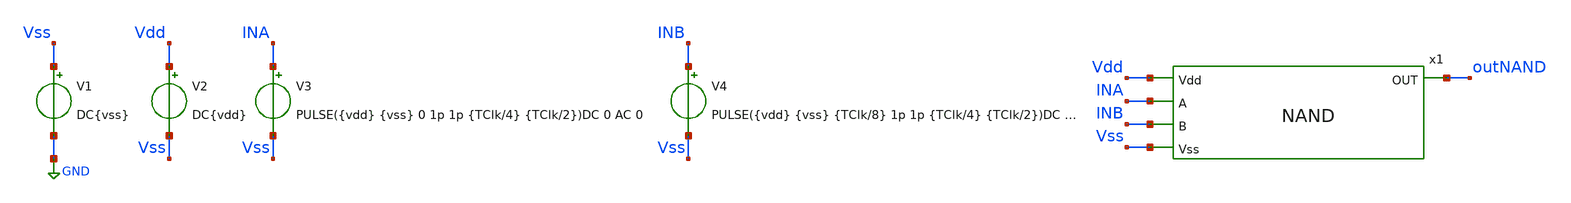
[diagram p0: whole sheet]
** sch_path: icdesign/sch/NAND/tb_NAND.sch
**.subckt tb_NAND
V1 Vss GND DC{vss}
V2 Vdd Vss DC{vdd}
V3 INA Vss PULSE({vdd} {vss} 0 1p 1p {TClk/4} {TClk/2})DC 0 AC 0
V4 INB Vss PULSE({vdd} {vss} {TClk/8} 1p 1p {TClk/4} {TClk/2})DC 0 AC 0
x1 Vdd INA INB outNAND Vss NAND
**** begin user architecture code





* Circuit Parameters
.param vdd  = 1.8
.param vss  = 0.0
.param Tclk = 10n
.options TEMP = 65.0


* Include Models
.lib ~/skywater/skywater-pdk/libraries/sky130_fd_pr_ngspice/latest/models/corners/sky130.lib TT


* OP Parameters & Singals to save
.save all


*Simulations
.control
  tran 0.01u 100n
  setplot tran1
  plot v(INA)v(INB)+2 v(outNAND)+4
.endc
.end


**** end user architecture code
**.ends

* expanding   symbol:  NAND/NAND.sym # of pins=5
** sym_path: icdesign/sch/NAND/NAND.sym
** sch_path: icdesign/sch/NAND/NAND.sch
.subckt NAND Vdd A B OUT Vss
*.ipin A
*.ipin B
*.ipin Vdd
*.ipin Vss
*.opin OUT
XM1 net1 B Vss Vss sky130_fd_pr__nfet_01v8 L=0.15 W=0.75 nf=1 ad='int((nf+1)/2) * W/nf * 0.29' as='int((nf+2)/2) * W/nf * 0.29'
+ pd='2*int((nf+1)/2) * (W/nf + 0.29)' ps='2*int((nf+2)/2) * (W/nf + 0.29)' nrd='0.29 / W' nrs='0.29 / W'
+ sa=0 sb=0 sd=0 mult=2 m=2
XM2 OUT A net1 Vss sky130_fd_pr__nfet_01v8 L=0.15 W=0.75 nf=1 ad='int((nf+1)/2) * W/nf * 0.29' as='int((nf+2)/2) * W/nf * 0.29'
+ pd='2*int((nf+1)/2) * (W/nf + 0.29)' ps='2*int((nf+2)/2) * (W/nf + 0.29)' nrd='0.29 / W' nrs='0.29 / W'
+ sa=0 sb=0 sd=0 mult=2 m=2
XM5 OUT B Vdd Vdd sky130_fd_pr__pfet_01v8 L=0.15 W=0.75 nf=1 ad='int((nf+1)/2) * W/nf * 0.29' as='int((nf+2)/2) * W/nf * 0.29'
+ pd='2*int((nf+1)/2) * (W/nf + 0.29)' ps='2*int((nf+2)/2) * (W/nf + 0.29)' nrd='0.29 / W' nrs='0.29 / W'
+ sa=0 sb=0 sd=0 mult=2 m=2
XM4 OUT A Vdd Vdd sky130_fd_pr__pfet_01v8 L=0.15 W=0.75 nf=1 ad='int((nf+1)/2) * W/nf * 0.29' as='int((nf+2)/2) * W/nf * 0.29'
+ pd='2*int((nf+1)/2) * (W/nf + 0.29)' ps='2*int((nf+2)/2) * (W/nf + 0.29)' nrd='0.29 / W' nrs='0.29 / W'
+ sa=0 sb=0 sd=0 mult=2 m=2
.ends

.GLOBAL GND
.end
